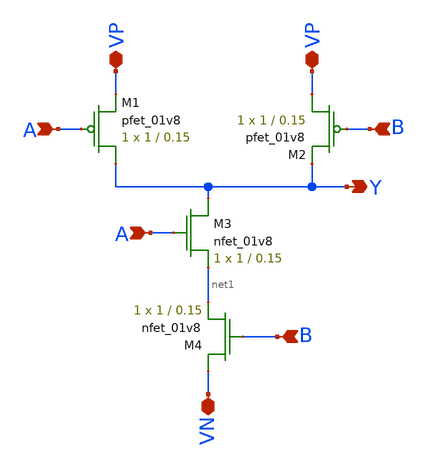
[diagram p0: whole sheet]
** sch_path: nand.sch
**.subckt nand VP VP Y A B VN A B
*.iopin VP
*.iopin VP
*.opin Y
*.ipin A
*.ipin B
*.iopin VN
*.ipin A
*.ipin B
XM1 Y A VP VDD sky130_fd_pr__pfet_01v8 L=0.15 W=1 nf=1 ad='int((nf+1)/2) * W/nf * 0.29' as='int((nf+2)/2) * W/nf * 0.29'
+ pd='2*int((nf+1)/2) * (W/nf + 0.29)' ps='2*int((nf+2)/2) * (W/nf + 0.29)' nrd='0.29 / W' nrs='0.29 / W'
+ sa=0 sb=0 sd=0 mult=1 m=1
XM2 VP B Y VDD sky130_fd_pr__pfet_01v8 L=0.15 W=1 nf=1 ad='int((nf+1)/2) * W/nf * 0.29' as='int((nf+2)/2) * W/nf * 0.29'
+ pd='2*int((nf+1)/2) * (W/nf + 0.29)' ps='2*int((nf+2)/2) * (W/nf + 0.29)' nrd='0.29 / W' nrs='0.29 / W'
+ sa=0 sb=0 sd=0 mult=1 m=1
XM3 Y A net1 GND sky130_fd_pr__nfet_01v8 L=0.15 W=1 nf=1 ad='int((nf+1)/2) * W/nf * 0.29' as='int((nf+2)/2) * W/nf * 0.29'
+ pd='2*int((nf+1)/2) * (W/nf + 0.29)' ps='2*int((nf+2)/2) * (W/nf + 0.29)' nrd='0.29 / W' nrs='0.29 / W'
+ sa=0 sb=0 sd=0 mult=1 m=1
XM4 VN B net1 GND sky130_fd_pr__nfet_01v8 L=0.15 W=1 nf=1 ad='int((nf+1)/2) * W/nf * 0.29' as='int((nf+2)/2) * W/nf * 0.29'
+ pd='2*int((nf+1)/2) * (W/nf + 0.29)' ps='2*int((nf+2)/2) * (W/nf + 0.29)' nrd='0.29 / W' nrs='0.29 / W'
+ sa=0 sb=0 sd=0 mult=1 m=1
**.ends
.end
